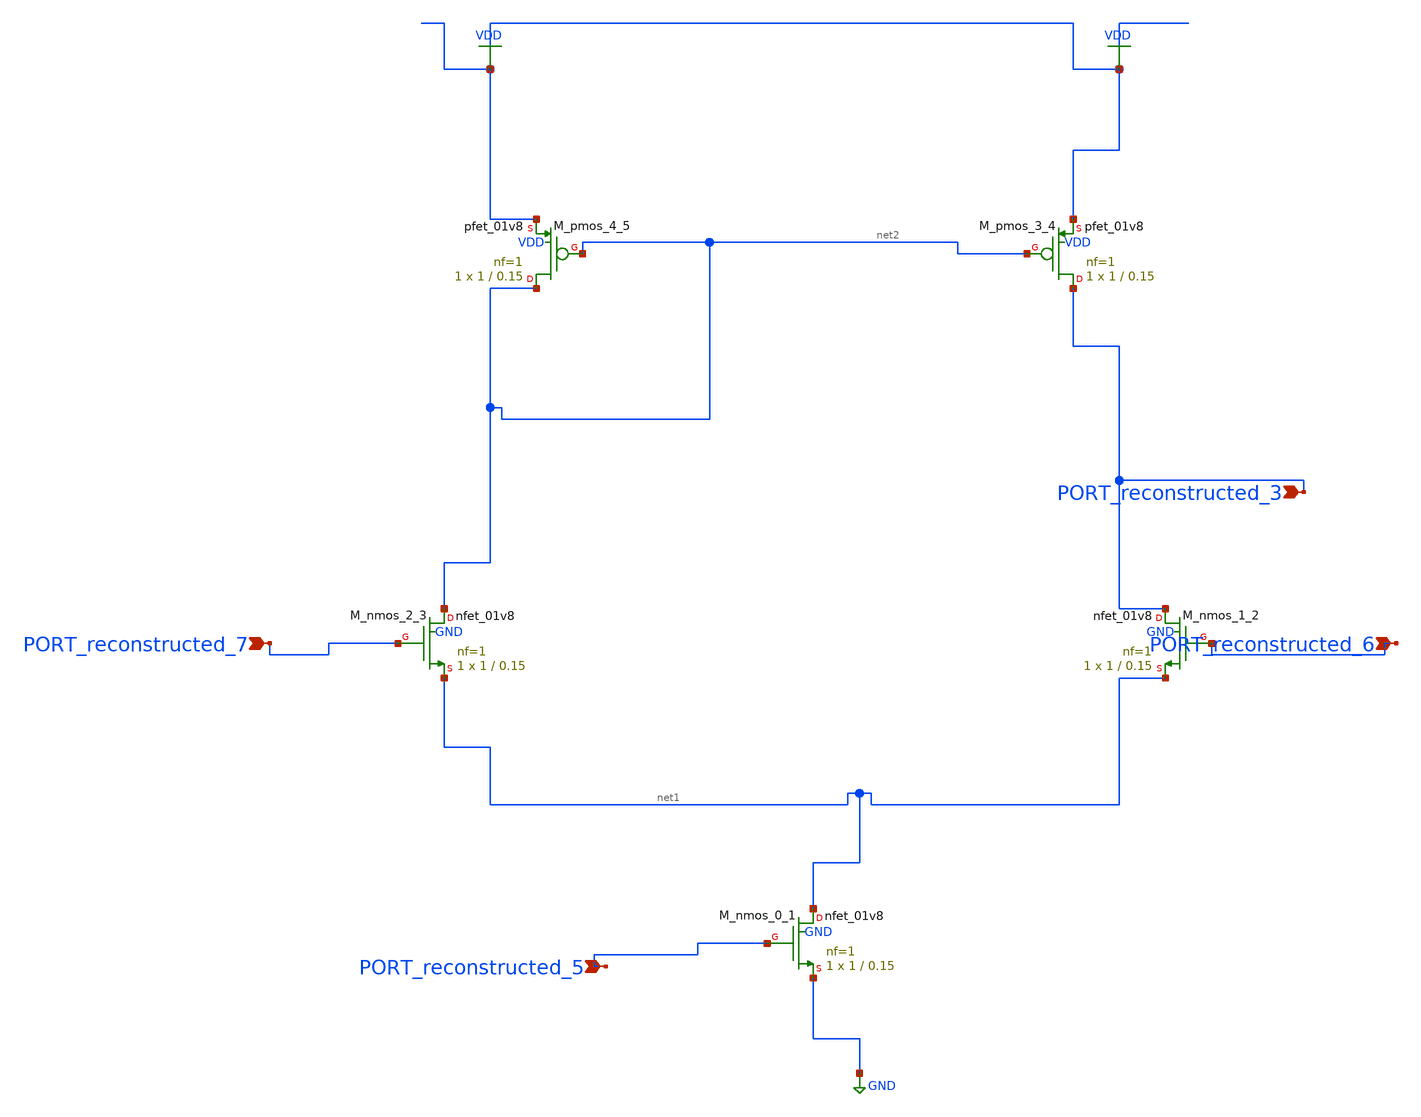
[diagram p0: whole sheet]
** sch_path: schematics/AMSNet/277.sch
**.subckt 277 PORT_reconstructed_5 PORT_reconstructed_3 PORT_reconstructed_6 PORT_reconstructed_7
*.ipin PORT_reconstructed_5
*.ipin PORT_reconstructed_3
*.ipin PORT_reconstructed_6
*.ipin PORT_reconstructed_7
XM_nmos_0_1 net1 PORT_reconstructed_5 GND GND sky130_fd_pr__nfet_01v8 L=0.15 W=1 nf=1 ad='int((1 + 1)/2) * 1 / 1 * 0.29'
+ as='int((1 + 2)/2) * 1 / 1 * 0.29' pd='2*int((1 + 1)/2) * (1 / 1 + 0.29)' ps='2*int((1 + 2)/2) * (1 / 1 + 0.29)'
+ nrd='0.29 / 1 ' nrs='0.29 / 1 ' sa=0 sb=0 sd=0 mult=1 m=1
XM_nmos_1_2 PORT_reconstructed_3 PORT_reconstructed_6 net1 GND sky130_fd_pr__nfet_01v8 L=0.15 W=1 nf=1
+ ad='int((1 + 1)/2) * 1 / 1 * 0.29' as='int((1 + 2)/2) * 1 / 1 * 0.29' pd='2*int((1 + 1)/2) * (1 / 1 + 0.29)'
+ ps='2*int((1 + 2)/2) * (1 / 1 + 0.29)' nrd='0.29 / 1 ' nrs='0.29 / 1 ' sa=0 sb=0 sd=0 mult=1 m=1
XM_nmos_2_3 net2 PORT_reconstructed_7 net1 GND sky130_fd_pr__nfet_01v8 L=0.15 W=1 nf=1 ad='int((1 + 1)/2) * 1 / 1 * 0.29'
+ as='int((1 + 2)/2) * 1 / 1 * 0.29' pd='2*int((1 + 1)/2) * (1 / 1 + 0.29)' ps='2*int((1 + 2)/2) * (1 / 1 + 0.29)'
+ nrd='0.29 / 1 ' nrs='0.29 / 1 ' sa=0 sb=0 sd=0 mult=1 m=1
XM_pmos_3_4 PORT_reconstructed_3 net2 VDD VDD sky130_fd_pr__pfet_01v8 L=0.15 W=1 nf=1 ad='int((1 + 1)/2) * 1 / 1 * 0.29'
+ as='int((1 + 2)/2) * 1 / 1 * 0.29' pd='2*int((1 + 1)/2) * (1 / 1 + 0.29)' ps='2*int((1 + 2)/2) * (1 / 1 + 0.29)'
+ nrd='0.29 / 1 ' nrs='0.29 / 1 ' sa=0 sb=0 sd=0 mult=1 m=1
XM_pmos_4_5 net2 net2 VDD VDD sky130_fd_pr__pfet_01v8 L=0.15 W=1 nf=1 ad='int((1 + 1)/2) * 1 / 1 * 0.29'
+ as='int((1 + 2)/2) * 1 / 1 * 0.29' pd='2*int((1 + 1)/2) * (1 / 1 + 0.29)' ps='2*int((1 + 2)/2) * (1 / 1 + 0.29)'
+ nrd='0.29 / 1 ' nrs='0.29 / 1 ' sa=0 sb=0 sd=0 mult=1 m=1
**.ends
.GLOBAL GND
.GLOBAL VDD
.end
